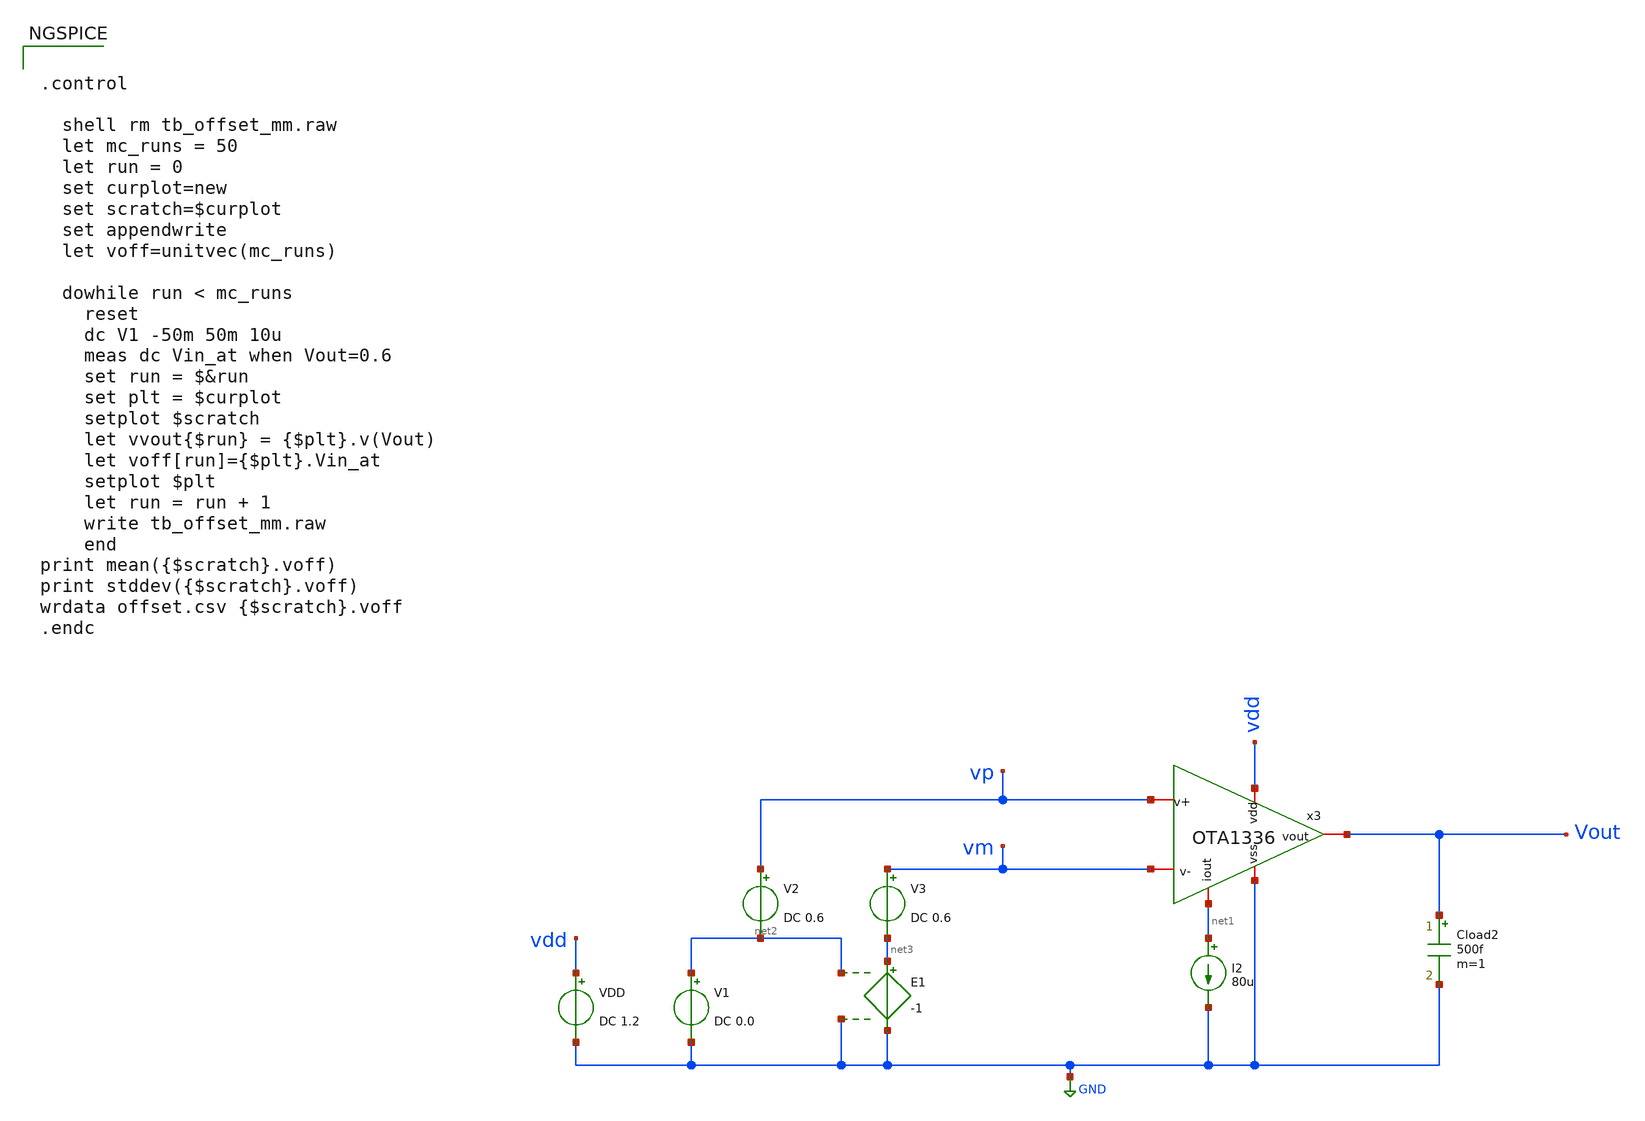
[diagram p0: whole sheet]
** sch_path: tests/data/OTA1336/testbenches/mm/xschem/OTA1336_offset-mm.sch
**.subckt OTA1336_offset-mm
VDD vdd GND DC 1.2
I2 net1 GND 80u
V1 net2 GND DC 0.0
x3 vdd net1 Vout vm vp GND OTA1336
Cload2 Vout GND 500f m=1
V2 vp net2 DC 0.6
V3 vm net3 DC 0.6
E1 net3 GND net2 GND -1
**** begin user architecture code

.lib cornerCAP.lib cap_typ
.lib cornerMOSlv.lib mos_tt_mismatch
.lib cornerRES.lib res_typ



.control

  shell rm tb_offset_mm.raw
  let mc_runs = 50
  let run = 0
  set curplot=new
  set scratch=$curplot
  set appendwrite
  let voff=unitvec(mc_runs)

  dowhile run < mc_runs
    reset
    dc V1 -50m 50m 10u
    meas dc Vin_at when Vout=0.6
    set run = $&run
    set plt = $curplot
    setplot $scratch
    let vvout{$run} = {$plt}.v(Vout)
    let voff[run]={$plt}.Vin_at
    setplot $plt
    let run = run + 1
    write tb_offset_mm.raw
    end
print mean({$scratch}.voff)
print stddev({$scratch}.voff)
wrdata offset.csv {$scratch}.voff
.endc


**** end user architecture code
**.ends
.GLOBAL GND
.end
